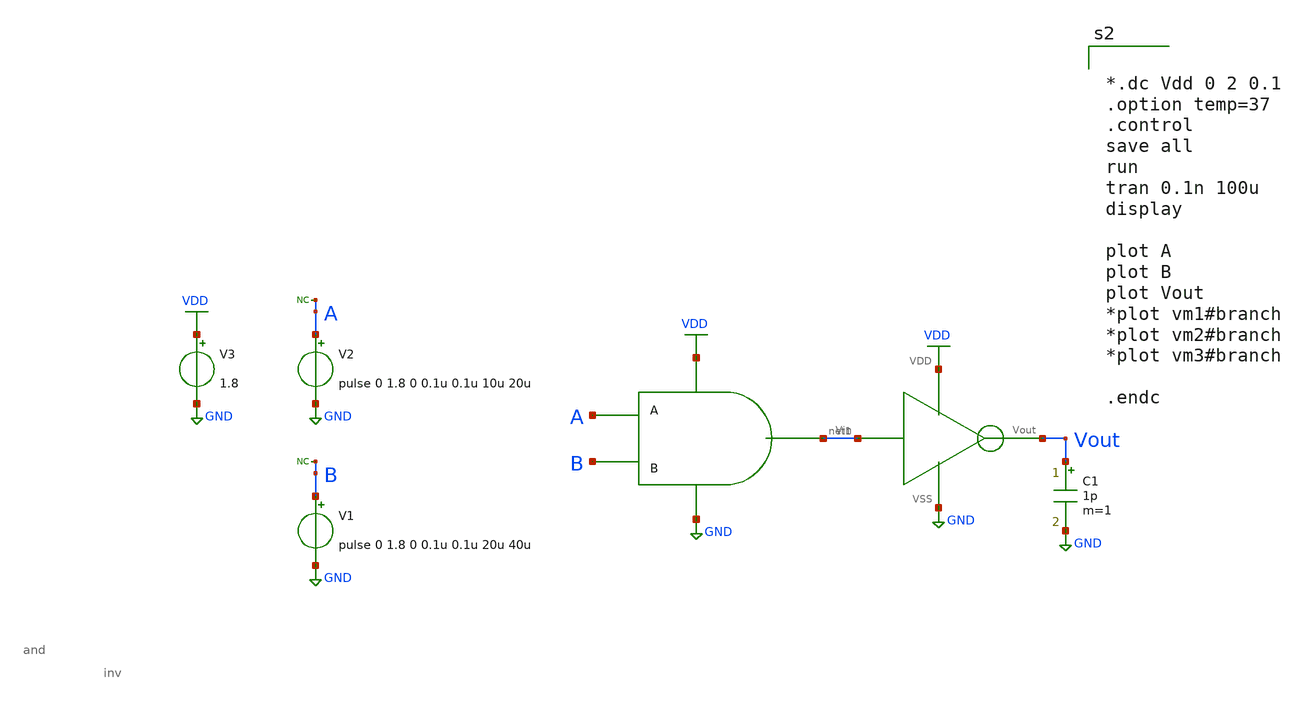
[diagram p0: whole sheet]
** sch_path: xschem/ip_block/logic_gate/tb_and.sch
**.subckt tb_and
V1 B GND pulse 0 1.8 0 0.1u 0.1u 20u 40u
* noconn B
V2 A GND pulse 0 1.8 0 0.1u 0.1u 10u 20u
* noconn A
X1 A net1 GND VDD B and
V3 VDD GND 1.8
C1 Vout GND 1p m=1
X2 net1 Vout GND VDD inv
**** begin user architecture code

** opencircuitdesign pdks install
.lib $::SKYWATER_MODELS/sky130.lib.spice tt




*.dc Vdd 0 2 0.1
.option temp=37
.control
save all
run
tran 0.1n 100u
display

plot A
plot B
plot Vout
*plot vm1#branch
*plot vm2#branch
*plot vm3#branch

.endc


**** end user architecture code
**.ends
.GLOBAL GND
.GLOBAL VDD
.end
